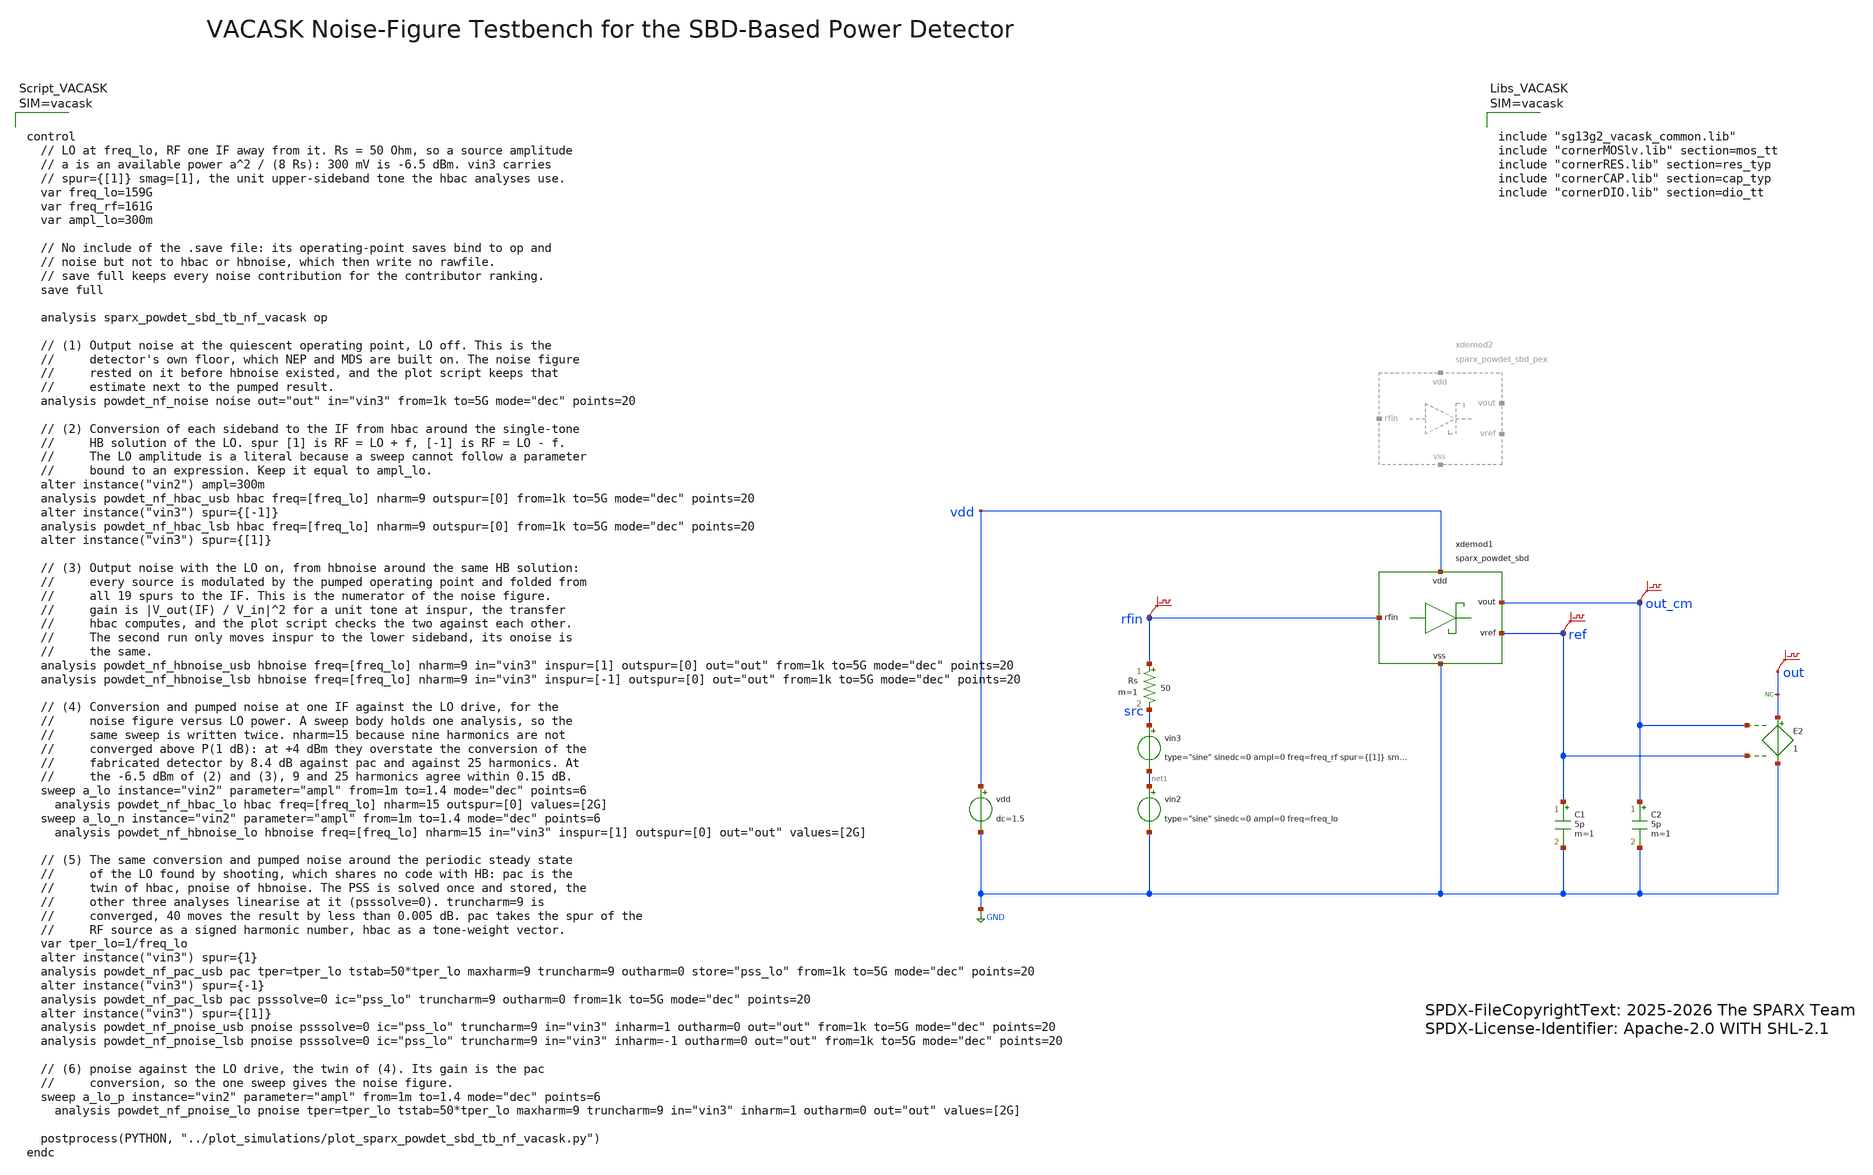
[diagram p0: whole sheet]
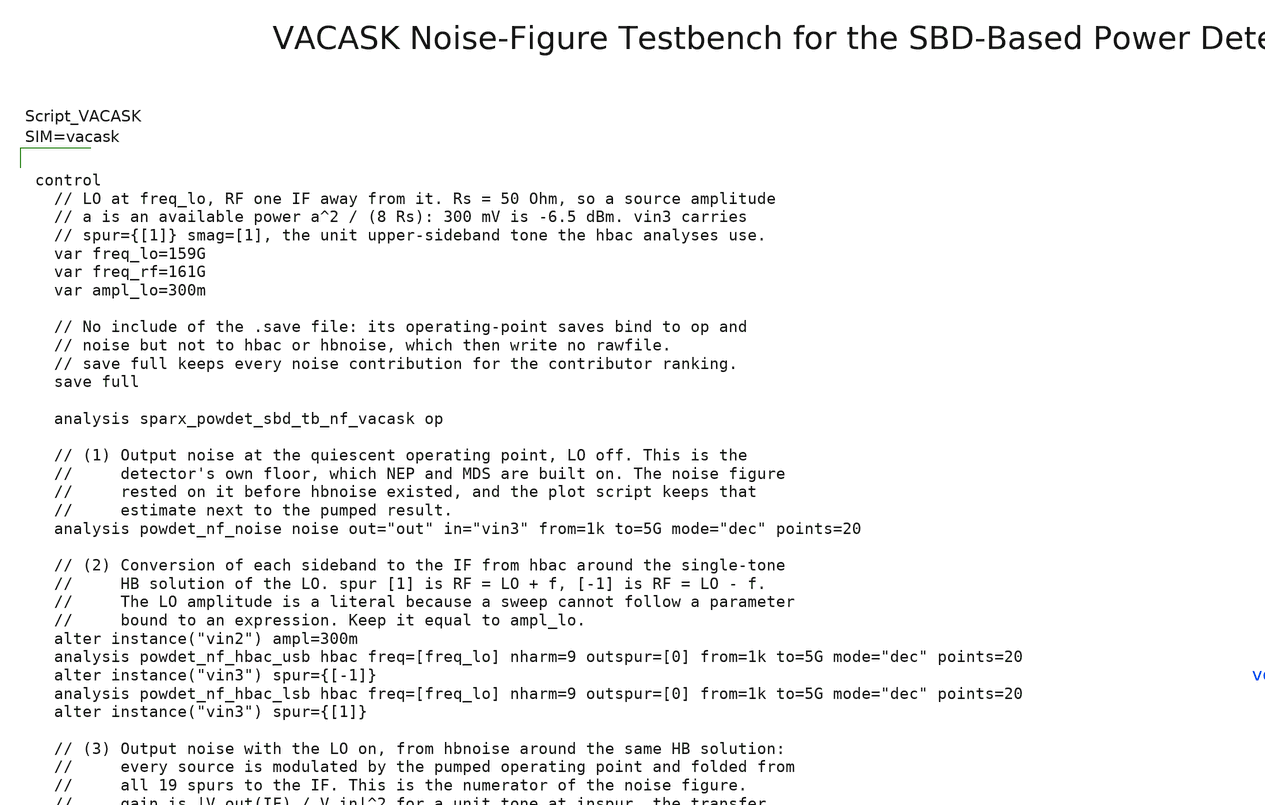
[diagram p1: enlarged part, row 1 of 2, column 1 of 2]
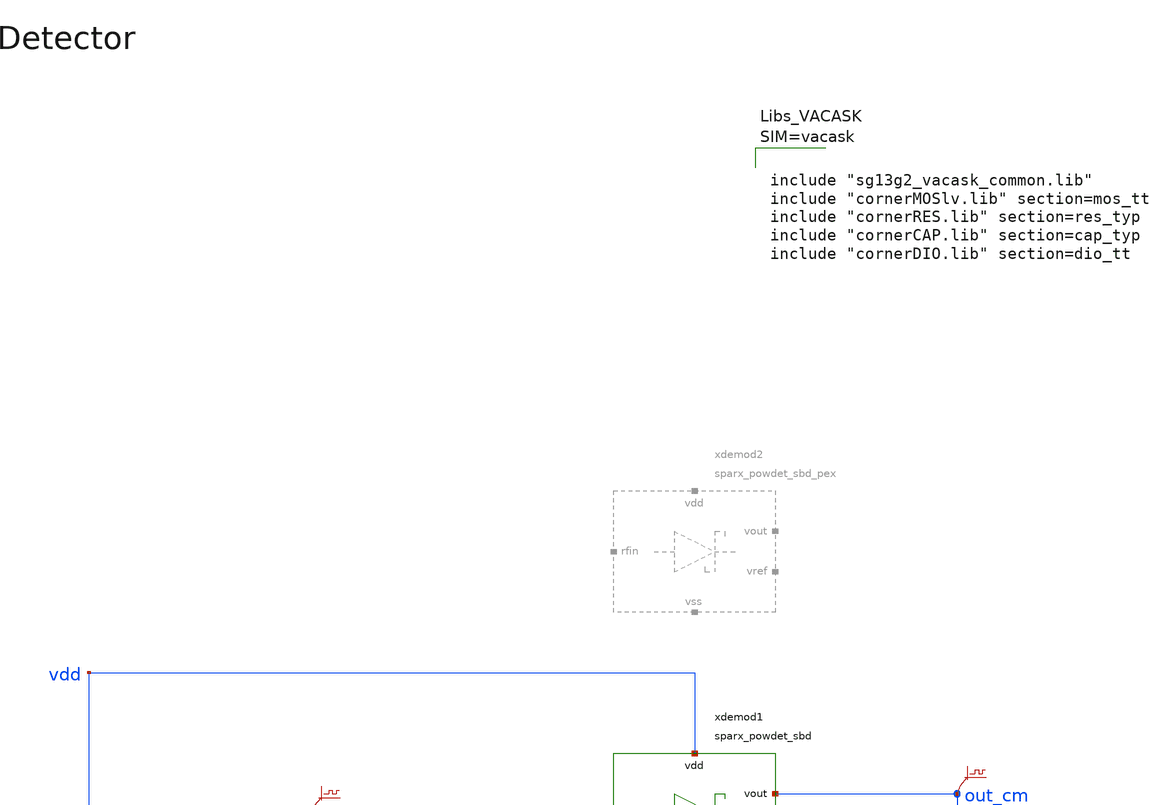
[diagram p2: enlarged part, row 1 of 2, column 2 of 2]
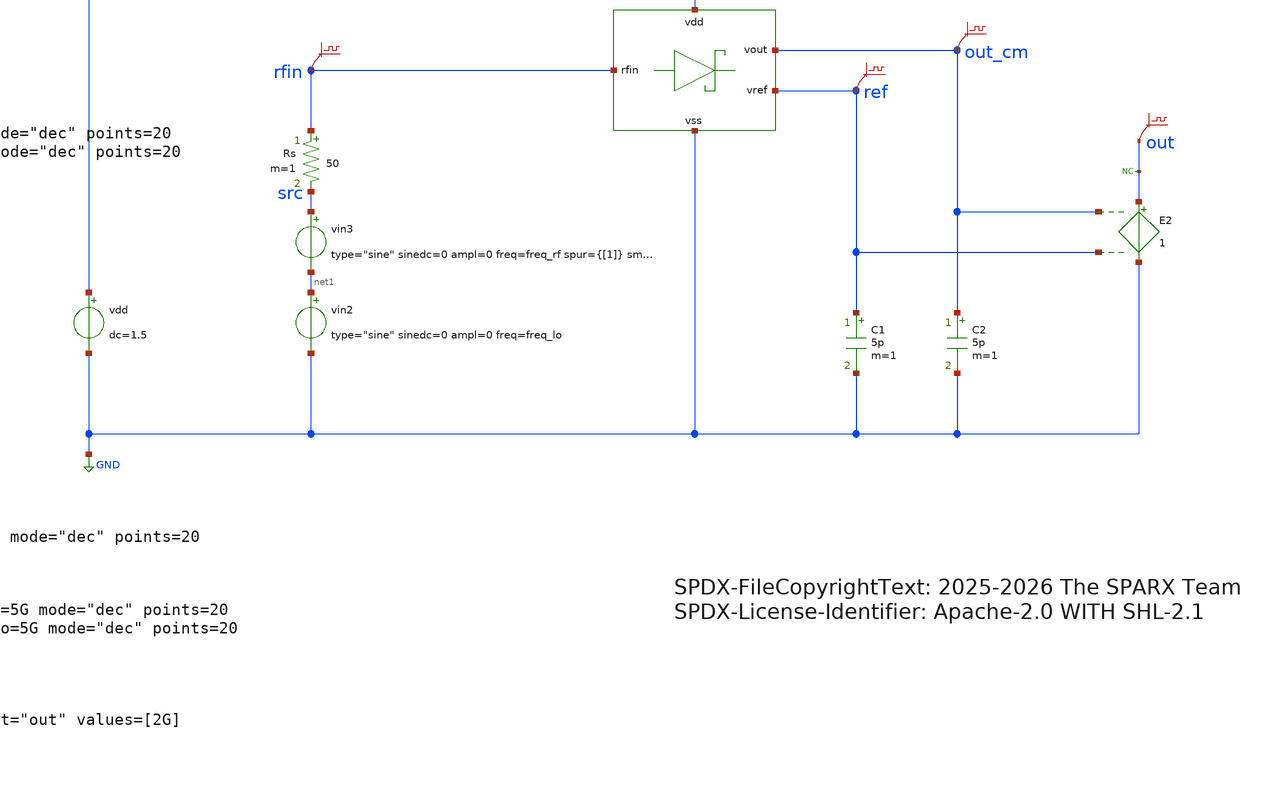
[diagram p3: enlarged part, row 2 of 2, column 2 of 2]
** sch_path: testbenches/xschem/sparx_powdet_sbd_tb_nf_vacask.sch
* SPDX-FileCopyrightText: 2025-2026 The SPARX Team
* SPDX-License-Identifier: Apache-2.0 WITH SHL-2.1
**.subckt sparx_powdet_sbd_tb_nf_vacask
vdd vdd GND dc=1.5
Rs rfin src 50 m=1
vin3 src net1 type="sine" sinedc=0 ampl=0 freq=freq_rf spur={[1]} smag=[1]
vin2 net1 GND type="sine" sinedc=0 ampl=0 freq=freq_lo
xdemod1 out_cm ref vdd rfin GND sparx_powdet_sbd
C1 ref GND 5p m=1
C2 out_cm GND 5p m=1
.save v(rfin)
.save v(out_cm)
.save v(ref)
E2 out GND out_cm ref 1
.save v(out)
* noconn out
**** begin user architecture code






**** end user architecture code
**.ends
.GLOBAL GND
.end
